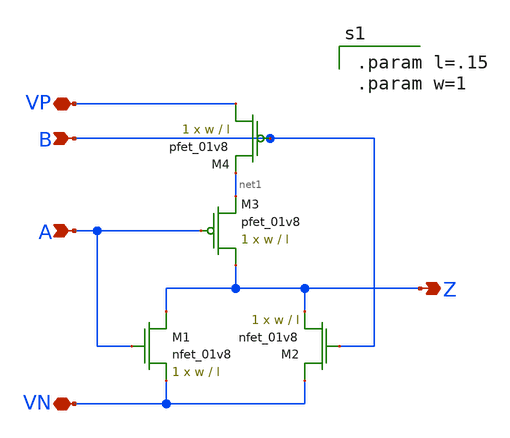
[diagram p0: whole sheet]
** sch_path: schematics/nor.sch
**.subckt nor A B VP VN Z
*.ipin A
*.ipin B
*.iopin VP
*.iopin VN
*.opin Z
XM1 Z A VN GND sky130_fd_pr__nfet_01v8 L=l W=w nf=1 ad='int((nf+1)/2) * W/nf * 0.29' as='int((nf+2)/2) * W/nf * 0.29'
+ pd='2*int((nf+1)/2) * (W/nf + 0.29)' ps='2*int((nf+2)/2) * (W/nf + 0.29)' nrd='0.29 / W' nrs='0.29 / W'
+ sa=0 sb=0 sd=0 mult=1 m=1
XM2 VN B Z GND sky130_fd_pr__nfet_01v8 L=l W=w nf=1 ad='int((nf+1)/2) * W/nf * 0.29' as='int((nf+2)/2) * W/nf * 0.29'
+ pd='2*int((nf+1)/2) * (W/nf + 0.29)' ps='2*int((nf+2)/2) * (W/nf + 0.29)' nrd='0.29 / W' nrs='0.29 / W'
+ sa=0 sb=0 sd=0 mult=1 m=1
XM3 Z A net1 VDD sky130_fd_pr__pfet_01v8 L=l W=w nf=1 ad='int((nf+1)/2) * W/nf * 0.29' as='int((nf+2)/2) * W/nf * 0.29'
+ pd='2*int((nf+1)/2) * (W/nf + 0.29)' ps='2*int((nf+2)/2) * (W/nf + 0.29)' nrd='0.29 / W' nrs='0.29 / W'
+ sa=0 sb=0 sd=0 mult=1 m=1
XM4 VP B net1 VDD sky130_fd_pr__pfet_01v8 L=l W=w nf=1 ad='int((nf+1)/2) * W/nf * 0.29' as='int((nf+2)/2) * W/nf * 0.29'
+ pd='2*int((nf+1)/2) * (W/nf + 0.29)' ps='2*int((nf+2)/2) * (W/nf + 0.29)' nrd='0.29 / W' nrs='0.29 / W'
+ sa=0 sb=0 sd=0 mult=1 m=1
**** begin user architecture code

.param l=.15
.param w=1

**** end user architecture code
**.ends
.end
